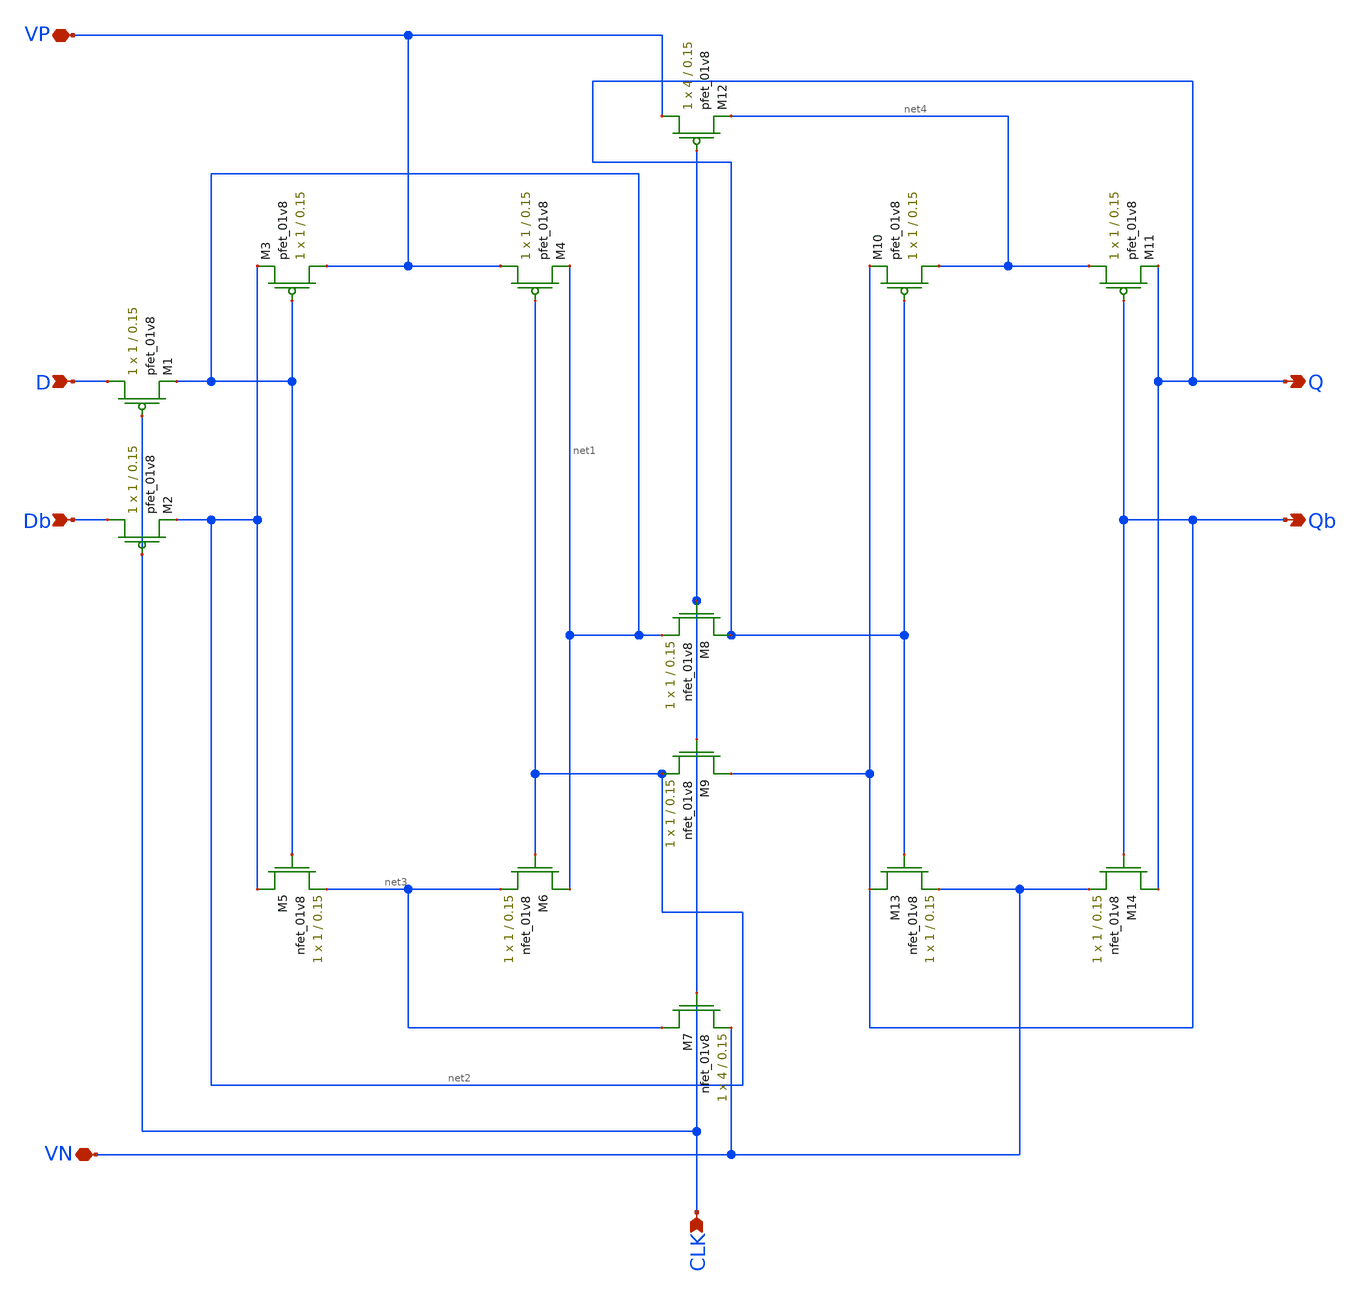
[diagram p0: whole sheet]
** sch_path: simulation/shift_register/andrew_mp2_files/d_flipflop/d_flipflop_LDS_Final.sch
**.subckt d_flipflop_LDS_Final D CLK Q Qb Db VP VN
*.ipin D
*.ipin CLK
*.opin Q
*.opin Qb
*.ipin Db
*.iopin VP
*.iopin VN
XM1 D CLK net1 VDD sky130_fd_pr__pfet_01v8 L=0.15 W=1 nf=1 ad='int((nf+1)/2) * W/nf * 0.29' as='int((nf+2)/2) * W/nf * 0.29'
+ pd='2*int((nf+1)/2) * (W/nf + 0.29)' ps='2*int((nf+2)/2) * (W/nf + 0.29)' nrd='0.29 / W' nrs='0.29 / W'
+ sa=0 sb=0 sd=0 mult=1 m=1
XM2 Db CLK net2 VDD sky130_fd_pr__pfet_01v8 L=0.15 W=1 nf=1 ad='int((nf+1)/2) * W/nf * 0.29' as='int((nf+2)/2) * W/nf * 0.29'
+ pd='2*int((nf+1)/2) * (W/nf + 0.29)' ps='2*int((nf+2)/2) * (W/nf + 0.29)' nrd='0.29 / W' nrs='0.29 / W'
+ sa=0 sb=0 sd=0 mult=1 m=1
XM3 VP net1 net2 VDD sky130_fd_pr__pfet_01v8 L=0.15 W=1 nf=1 ad='int((nf+1)/2) * W/nf * 0.29' as='int((nf+2)/2) * W/nf * 0.29'
+ pd='2*int((nf+1)/2) * (W/nf + 0.29)' ps='2*int((nf+2)/2) * (W/nf + 0.29)' nrd='0.29 / W' nrs='0.29 / W'
+ sa=0 sb=0 sd=0 mult=1 m=1
XM5 net2 net1 net3 GND sky130_fd_pr__nfet_01v8 L=0.15 W=1 nf=1 ad='int((nf+1)/2) * W/nf * 0.29' as='int((nf+2)/2) * W/nf * 0.29'
+ pd='2*int((nf+1)/2) * (W/nf + 0.29)' ps='2*int((nf+2)/2) * (W/nf + 0.29)' nrd='0.29 / W' nrs='0.29 / W'
+ sa=0 sb=0 sd=0 mult=1 m=1
XM7 net3 CLK VN GND sky130_fd_pr__nfet_01v8 L=0.15 W=4 nf=1 ad='int((nf+1)/2) * W/nf * 0.29' as='int((nf+2)/2) * W/nf * 0.29'
+ pd='2*int((nf+1)/2) * (W/nf + 0.29)' ps='2*int((nf+2)/2) * (W/nf + 0.29)' nrd='0.29 / W' nrs='0.29 / W'
+ sa=0 sb=0 sd=0 mult=1 m=1
XM8 Q CLK net1 GND sky130_fd_pr__nfet_01v8 L=0.15 W=1 nf=1 ad='int((nf+1)/2) * W/nf * 0.29' as='int((nf+2)/2) * W/nf * 0.29'
+ pd='2*int((nf+1)/2) * (W/nf + 0.29)' ps='2*int((nf+2)/2) * (W/nf + 0.29)' nrd='0.29 / W' nrs='0.29 / W'
+ sa=0 sb=0 sd=0 mult=1 m=1
XM9 Qb CLK net2 GND sky130_fd_pr__nfet_01v8 L=0.15 W=1 nf=1 ad='int((nf+1)/2) * W/nf * 0.29' as='int((nf+2)/2) * W/nf * 0.29'
+ pd='2*int((nf+1)/2) * (W/nf + 0.29)' ps='2*int((nf+2)/2) * (W/nf + 0.29)' nrd='0.29 / W' nrs='0.29 / W'
+ sa=0 sb=0 sd=0 mult=1 m=1
XM10 net4 Q Qb VDD sky130_fd_pr__pfet_01v8 L=0.15 W=1 nf=1 ad='int((nf+1)/2) * W/nf * 0.29' as='int((nf+2)/2) * W/nf * 0.29'
+ pd='2*int((nf+1)/2) * (W/nf + 0.29)' ps='2*int((nf+2)/2) * (W/nf + 0.29)' nrd='0.29 / W' nrs='0.29 / W'
+ sa=0 sb=0 sd=0 mult=1 m=1
XM11 net4 Qb Q VDD sky130_fd_pr__pfet_01v8 L=0.15 W=1 nf=1 ad='int((nf+1)/2) * W/nf * 0.29' as='int((nf+2)/2) * W/nf * 0.29'
+ pd='2*int((nf+1)/2) * (W/nf + 0.29)' ps='2*int((nf+2)/2) * (W/nf + 0.29)' nrd='0.29 / W' nrs='0.29 / W'
+ sa=0 sb=0 sd=0 mult=1 m=1
XM12 VP CLK net4 VDD sky130_fd_pr__pfet_01v8 L=0.15 W=4 nf=1 ad='int((nf+1)/2) * W/nf * 0.29' as='int((nf+2)/2) * W/nf * 0.29'
+ pd='2*int((nf+1)/2) * (W/nf + 0.29)' ps='2*int((nf+2)/2) * (W/nf + 0.29)' nrd='0.29 / W' nrs='0.29 / W'
+ sa=0 sb=0 sd=0 mult=1 m=1
XM13 Qb Q VN GND sky130_fd_pr__nfet_01v8 L=0.15 W=1 nf=1 ad='int((nf+1)/2) * W/nf * 0.29' as='int((nf+2)/2) * W/nf * 0.29'
+ pd='2*int((nf+1)/2) * (W/nf + 0.29)' ps='2*int((nf+2)/2) * (W/nf + 0.29)' nrd='0.29 / W' nrs='0.29 / W'
+ sa=0 sb=0 sd=0 mult=1 m=1
XM14 Q Qb VN GND sky130_fd_pr__nfet_01v8 L=0.15 W=1 nf=1 ad='int((nf+1)/2) * W/nf * 0.29' as='int((nf+2)/2) * W/nf * 0.29'
+ pd='2*int((nf+1)/2) * (W/nf + 0.29)' ps='2*int((nf+2)/2) * (W/nf + 0.29)' nrd='0.29 / W' nrs='0.29 / W'
+ sa=0 sb=0 sd=0 mult=1 m=1
XM4 VP net2 net1 VDD sky130_fd_pr__pfet_01v8 L=0.15 W=1 nf=1 ad='int((nf+1)/2) * W/nf * 0.29' as='int((nf+2)/2) * W/nf * 0.29'
+ pd='2*int((nf+1)/2) * (W/nf + 0.29)' ps='2*int((nf+2)/2) * (W/nf + 0.29)' nrd='0.29 / W' nrs='0.29 / W'
+ sa=0 sb=0 sd=0 mult=1 m=1
XM6 net1 net2 net3 GND sky130_fd_pr__nfet_01v8 L=0.15 W=1 nf=1 ad='int((nf+1)/2) * W/nf * 0.29' as='int((nf+2)/2) * W/nf * 0.29'
+ pd='2*int((nf+1)/2) * (W/nf + 0.29)' ps='2*int((nf+2)/2) * (W/nf + 0.29)' nrd='0.29 / W' nrs='0.29 / W'
+ sa=0 sb=0 sd=0 mult=1 m=1
**.ends
.end
